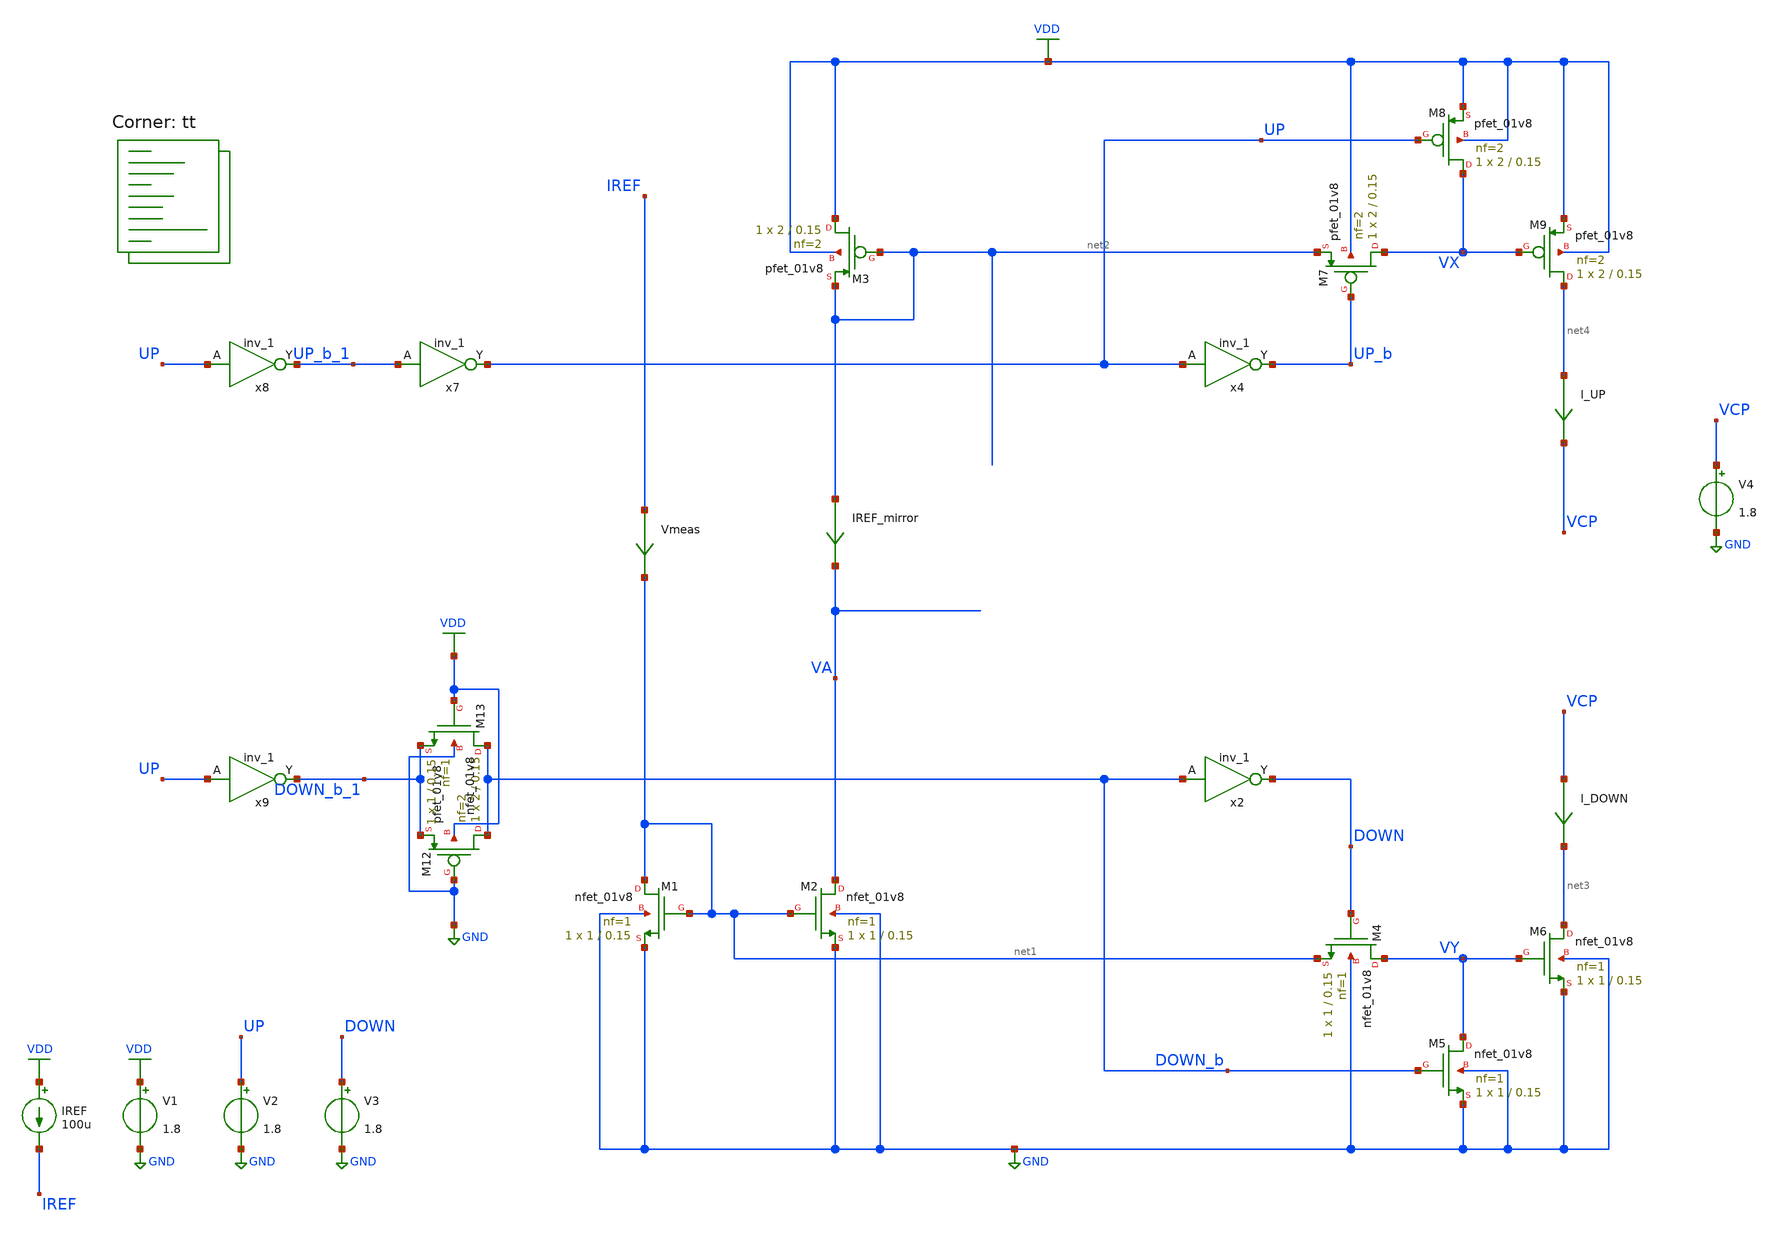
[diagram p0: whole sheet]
** sch_path: projects/pll/charge_pump/xschem_ngspice/charge_pump2.sch
**.subckt charge_pump2
XM1 net1 net1 GND GND sky130_fd_pr__nfet_01v8 L=0.15 W=1 nf=1 ad='int((nf+1)/2) * W/nf * 0.29' as='int((nf+2)/2) * W/nf * 0.29'
+ pd='2*int((nf+1)/2) * (W/nf + 0.29)' ps='2*int((nf+2)/2) * (W/nf + 0.29)' nrd='0.29 / W' nrs='0.29 / W'
+ sa=0 sb=0 sd=0 mult=1 m=1
XM2 VA net1 GND GND sky130_fd_pr__nfet_01v8 L=0.15 W=1 nf=1 ad='int((nf+1)/2) * W/nf * 0.29' as='int((nf+2)/2) * W/nf * 0.29'
+ pd='2*int((nf+1)/2) * (W/nf + 0.29)' ps='2*int((nf+2)/2) * (W/nf + 0.29)' nrd='0.29 / W' nrs='0.29 / W'
+ sa=0 sb=0 sd=0 mult=1 m=1
XM4 VY DOWN net1 GND sky130_fd_pr__nfet_01v8 L=0.15 W=1 nf=1 ad='int((nf+1)/2) * W/nf * 0.29' as='int((nf+2)/2) * W/nf * 0.29'
+ pd='2*int((nf+1)/2) * (W/nf + 0.29)' ps='2*int((nf+2)/2) * (W/nf + 0.29)' nrd='0.29 / W' nrs='0.29 / W'
+ sa=0 sb=0 sd=0 mult=1 m=1
XM5 VY DOWN_b GND GND sky130_fd_pr__nfet_01v8 L=0.15 W=1 nf=1 ad='int((nf+1)/2) * W/nf * 0.29' as='int((nf+2)/2) * W/nf * 0.29'
+ pd='2*int((nf+1)/2) * (W/nf + 0.29)' ps='2*int((nf+2)/2) * (W/nf + 0.29)' nrd='0.29 / W' nrs='0.29 / W'
+ sa=0 sb=0 sd=0 mult=1 m=1
XM6 net3 VY GND GND sky130_fd_pr__nfet_01v8 L=0.15 W=1 nf=1 ad='int((nf+1)/2) * W/nf * 0.29' as='int((nf+2)/2) * W/nf * 0.29'
+ pd='2*int((nf+1)/2) * (W/nf + 0.29)' ps='2*int((nf+2)/2) * (W/nf + 0.29)' nrd='0.29 / W' nrs='0.29 / W'
+ sa=0 sb=0 sd=0 mult=1 m=1
XM3 VDD net2 net2 VDD sky130_fd_pr__pfet_01v8 L=0.15 W=2 nf=2 ad='int((nf+1)/2) * W/nf * 0.29' as='int((nf+2)/2) * W/nf * 0.29'
+ pd='2*int((nf+1)/2) * (W/nf + 0.29)' ps='2*int((nf+2)/2) * (W/nf + 0.29)' nrd='0.29 / W' nrs='0.29 / W'
+ sa=0 sb=0 sd=0 mult=1 m=1
XM7 VX UP_b net2 VDD sky130_fd_pr__pfet_01v8 L=0.15 W=2 nf=2 ad='int((nf+1)/2) * W/nf * 0.29' as='int((nf+2)/2) * W/nf * 0.29'
+ pd='2*int((nf+1)/2) * (W/nf + 0.29)' ps='2*int((nf+2)/2) * (W/nf + 0.29)' nrd='0.29 / W' nrs='0.29 / W'
+ sa=0 sb=0 sd=0 mult=1 m=1
XM8 VX UP VDD VDD sky130_fd_pr__pfet_01v8 L=0.15 W=2 nf=2 ad='int((nf+1)/2) * W/nf * 0.29' as='int((nf+2)/2) * W/nf * 0.29'
+ pd='2*int((nf+1)/2) * (W/nf + 0.29)' ps='2*int((nf+2)/2) * (W/nf + 0.29)' nrd='0.29 / W' nrs='0.29 / W'
+ sa=0 sb=0 sd=0 mult=1 m=1
XM9 net4 VX VDD VDD sky130_fd_pr__pfet_01v8 L=0.15 W=2 nf=2 ad='int((nf+1)/2) * W/nf * 0.29' as='int((nf+2)/2) * W/nf * 0.29'
+ pd='2*int((nf+1)/2) * (W/nf + 0.29)' ps='2*int((nf+2)/2) * (W/nf + 0.29)' nrd='0.29 / W' nrs='0.29 / W'
+ sa=0 sb=0 sd=0 mult=1 m=1
IREF VDD IREF 100u
V1 VDD GND 1.8
x4 UP GND GND VDD VDD UP_b sky130_fd_sc_hd__inv_1
x2 DOWN_b GND GND VDD VDD DOWN sky130_fd_sc_hd__inv_1
XM12 DOWN_b GND DOWN_b_1 VDD sky130_fd_pr__pfet_01v8 L=0.15 W=2 nf=2 ad='int((nf+1)/2) * W/nf * 0.29'
+ as='int((nf+2)/2) * W/nf * 0.29' pd='2*int((nf+1)/2) * (W/nf + 0.29)' ps='2*int((nf+2)/2) * (W/nf + 0.29)'
+ nrd='0.29 / W' nrs='0.29 / W' sa=0 sb=0 sd=0 mult=1 m=1
XM13 DOWN_b VDD DOWN_b_1 GND sky130_fd_pr__nfet_01v8 L=0.15 W=1 nf=1 ad='int((nf+1)/2) * W/nf * 0.29'
+ as='int((nf+2)/2) * W/nf * 0.29' pd='2*int((nf+1)/2) * (W/nf + 0.29)' ps='2*int((nf+2)/2) * (W/nf + 0.29)'
+ nrd='0.29 / W' nrs='0.29 / W' sa=0 sb=0 sd=0 mult=1 m=1
x7 UP_b_1 GND GND VDD VDD UP sky130_fd_sc_hd__inv_1
x8 UP GND GND VDD VDD UP_b_1 sky130_fd_sc_hd__inv_1
x9 UP GND GND VDD VDD DOWN_b_1 sky130_fd_sc_hd__inv_1
V2 UP GND 1.8
V3 DOWN GND 1.8
IREF_mirror net2 VA 0
.save i(iref_mirror)
Vmeas IREF net1 0
.save i(vmeas)
V4 VCP GND 1.8
I_UP net4 VCP 0
.save i(i_up)
I_DOWN VCP net3 0
.save i(i_down)
**** begin user architecture code
.lib $::SKYWATER_MODELS/sky130.lib.spice tt



.include /foss/pdks/sky130A/libs.ref/sky130_fd_sc_hd/spice/sky130_fd_sc_hd.spice

.option method=gear trtol1
.option wnflag=1
* .option savecurrents

* .ic v(osc)=0
* .temp = 75

.save  @iout[current] @iref_mirror[current] @iref[current] @i_up[current] @i_down[current]


.control
  save v(va) v(vb) v(vx) v(vy) v(up) v(up_b) v(down) v(down_b) v(vref) v(vcp)
  * save all
  * tran 0.1ns 10us
  dc V2 0 1.8 1.8 V4 0 1.8 0.01
  remzerovec
  write charge_pump2.raw
  * wrdata /foss/designs/my_design/projects/pll/pfd/xschem_ngspice/charge_pump2_QA.txt v(osc)
  set appendwrite

.endc






**** end user architecture code
**.ends
.GLOBAL VDD
.GLOBAL GND
.end
